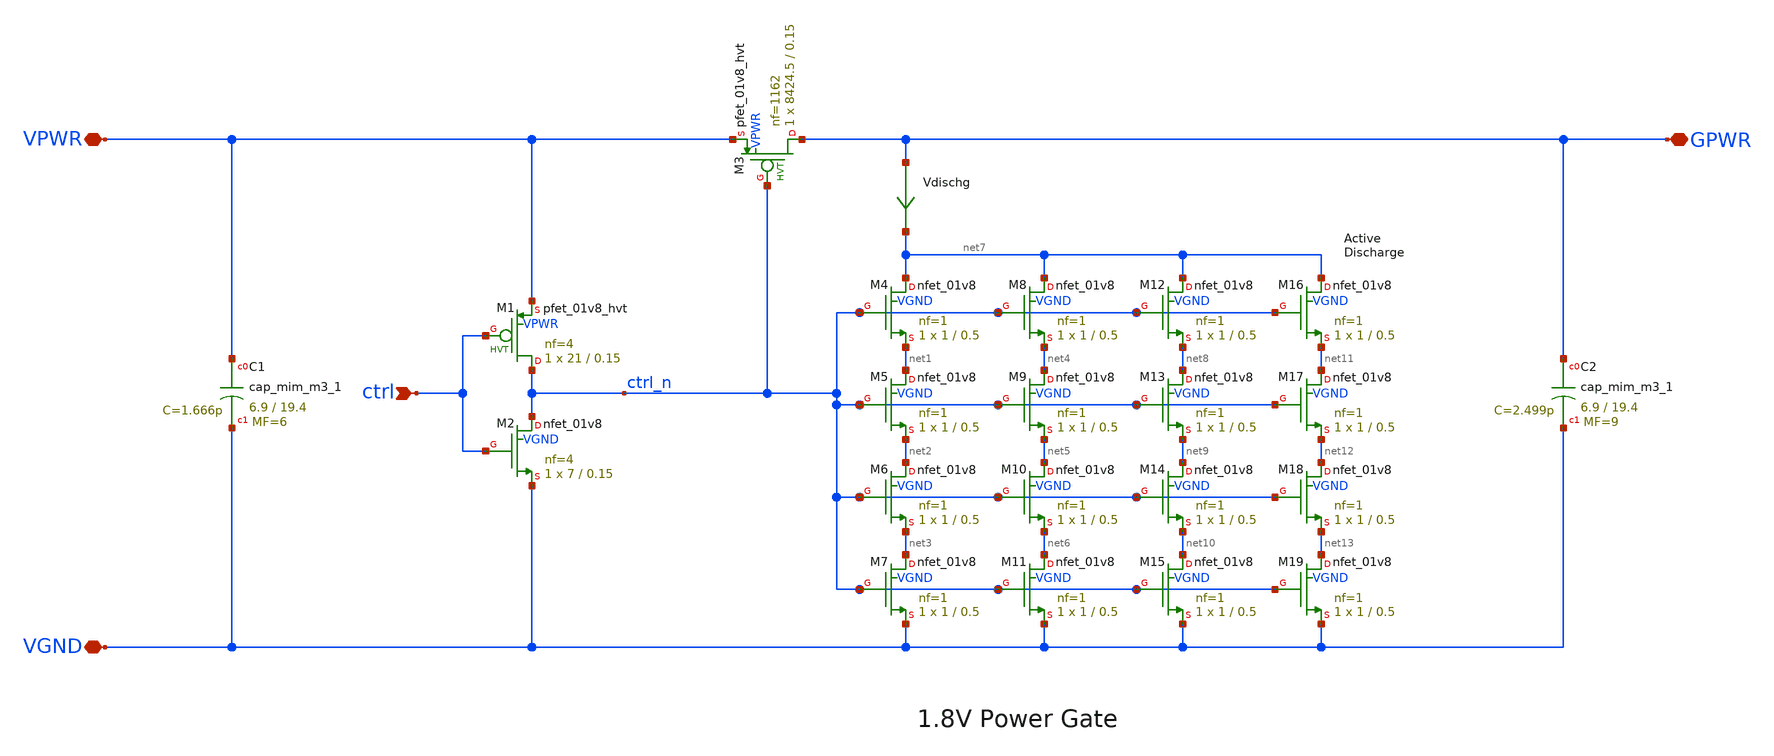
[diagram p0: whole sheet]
** sch_path: pg/sky130/tt_pg_1v8_ll_4/xschem/tt_pg_1v8_ll_4.sch
**.subckt tt_pg_1v8_ll_4 ctrl VGND VPWR GPWR
*.ipin ctrl
*.iopin VGND
*.iopin VPWR
*.iopin GPWR
XM2 ctrl_n ctrl VGND VGND sky130_fd_pr__nfet_01v8 L=0.15 W=7 nf=4 ad='int((nf+1)/2) * W/nf * 0.29' as='int((nf+2)/2) * W/nf * 0.29'
+ pd='2*int((nf+1)/2) * (W/nf + 0.29)' ps='2*int((nf+2)/2) * (W/nf + 0.29)' nrd='0.29 / W' nrs='0.29 / W'
+ sa=0 sb=0 sd=0 mult=1 m=1
XM1 ctrl_n ctrl VPWR VPWR sky130_fd_pr__pfet_01v8_hvt L=0.15 W=21 nf=4 ad='int((nf+1)/2) * W/nf * 0.29'
+ as='int((nf+2)/2) * W/nf * 0.29' pd='2*int((nf+1)/2) * (W/nf + 0.29)' ps='2*int((nf+2)/2) * (W/nf + 0.29)'
+ nrd='0.29 / W' nrs='0.29 / W' sa=0 sb=0 sd=0 mult=1 m=1
XM3 GPWR ctrl_n VPWR VPWR sky130_fd_pr__pfet_01v8_hvt L=0.15 W=8424.5 nf=1162 ad='int((nf+1)/2) * W/nf * 0.29'
+ as='int((nf+2)/2) * W/nf * 0.29' pd='2*int((nf+1)/2) * (W/nf + 0.29)' ps='2*int((nf+2)/2) * (W/nf + 0.29)'
+ nrd='0.29 / W' nrs='0.29 / W' sa=0 sb=0 sd=0 mult=1 m=1
XM4 net7 ctrl_n net1 VGND sky130_fd_pr__nfet_01v8 L=0.5 W=1 nf=1 ad='int((nf+1)/2) * W/nf * 0.29' as='int((nf+2)/2) * W/nf * 0.29'
+ pd='2*int((nf+1)/2) * (W/nf + 0.29)' ps='2*int((nf+2)/2) * (W/nf + 0.29)' nrd='0.29 / W' nrs='0.29 / W'
+ sa=0 sb=0 sd=0 mult=1 m=1
Vdischg GPWR net7 0
.save i(vdischg)
XM5 net1 ctrl_n net2 VGND sky130_fd_pr__nfet_01v8 L=0.5 W=1 nf=1 ad='int((nf+1)/2) * W/nf * 0.29' as='int((nf+2)/2) * W/nf * 0.29'
+ pd='2*int((nf+1)/2) * (W/nf + 0.29)' ps='2*int((nf+2)/2) * (W/nf + 0.29)' nrd='0.29 / W' nrs='0.29 / W'
+ sa=0 sb=0 sd=0 mult=1 m=1
XM6 net2 ctrl_n net3 VGND sky130_fd_pr__nfet_01v8 L=0.5 W=1 nf=1 ad='int((nf+1)/2) * W/nf * 0.29' as='int((nf+2)/2) * W/nf * 0.29'
+ pd='2*int((nf+1)/2) * (W/nf + 0.29)' ps='2*int((nf+2)/2) * (W/nf + 0.29)' nrd='0.29 / W' nrs='0.29 / W'
+ sa=0 sb=0 sd=0 mult=1 m=1
XM7 net3 ctrl_n VGND VGND sky130_fd_pr__nfet_01v8 L=0.5 W=1 nf=1 ad='int((nf+1)/2) * W/nf * 0.29' as='int((nf+2)/2) * W/nf * 0.29'
+ pd='2*int((nf+1)/2) * (W/nf + 0.29)' ps='2*int((nf+2)/2) * (W/nf + 0.29)' nrd='0.29 / W' nrs='0.29 / W'
+ sa=0 sb=0 sd=0 mult=1 m=1
XM8 net7 ctrl_n net4 VGND sky130_fd_pr__nfet_01v8 L=0.5 W=1 nf=1 ad='int((nf+1)/2) * W/nf * 0.29' as='int((nf+2)/2) * W/nf * 0.29'
+ pd='2*int((nf+1)/2) * (W/nf + 0.29)' ps='2*int((nf+2)/2) * (W/nf + 0.29)' nrd='0.29 / W' nrs='0.29 / W'
+ sa=0 sb=0 sd=0 mult=1 m=1
XM9 net4 ctrl_n net5 VGND sky130_fd_pr__nfet_01v8 L=0.5 W=1 nf=1 ad='int((nf+1)/2) * W/nf * 0.29' as='int((nf+2)/2) * W/nf * 0.29'
+ pd='2*int((nf+1)/2) * (W/nf + 0.29)' ps='2*int((nf+2)/2) * (W/nf + 0.29)' nrd='0.29 / W' nrs='0.29 / W'
+ sa=0 sb=0 sd=0 mult=1 m=1
XM10 net5 ctrl_n net6 VGND sky130_fd_pr__nfet_01v8 L=0.5 W=1 nf=1 ad='int((nf+1)/2) * W/nf * 0.29' as='int((nf+2)/2) * W/nf * 0.29'
+ pd='2*int((nf+1)/2) * (W/nf + 0.29)' ps='2*int((nf+2)/2) * (W/nf + 0.29)' nrd='0.29 / W' nrs='0.29 / W'
+ sa=0 sb=0 sd=0 mult=1 m=1
XM11 net6 ctrl_n VGND VGND sky130_fd_pr__nfet_01v8 L=0.5 W=1 nf=1 ad='int((nf+1)/2) * W/nf * 0.29' as='int((nf+2)/2) * W/nf * 0.29'
+ pd='2*int((nf+1)/2) * (W/nf + 0.29)' ps='2*int((nf+2)/2) * (W/nf + 0.29)' nrd='0.29 / W' nrs='0.29 / W'
+ sa=0 sb=0 sd=0 mult=1 m=1
XC1 VPWR VGND sky130_fd_pr__cap_mim_m3_1 W=6.9 L=19.4 MF=6 m=6
XC2 GPWR VGND sky130_fd_pr__cap_mim_m3_1 W=6.9 L=19.4 MF=9 m=9
XM12 net7 ctrl_n net8 VGND sky130_fd_pr__nfet_01v8 L=0.5 W=1 nf=1 ad='int((nf+1)/2) * W/nf * 0.29' as='int((nf+2)/2) * W/nf * 0.29'
+ pd='2*int((nf+1)/2) * (W/nf + 0.29)' ps='2*int((nf+2)/2) * (W/nf + 0.29)' nrd='0.29 / W' nrs='0.29 / W'
+ sa=0 sb=0 sd=0 mult=1 m=1
XM13 net8 ctrl_n net9 VGND sky130_fd_pr__nfet_01v8 L=0.5 W=1 nf=1 ad='int((nf+1)/2) * W/nf * 0.29' as='int((nf+2)/2) * W/nf * 0.29'
+ pd='2*int((nf+1)/2) * (W/nf + 0.29)' ps='2*int((nf+2)/2) * (W/nf + 0.29)' nrd='0.29 / W' nrs='0.29 / W'
+ sa=0 sb=0 sd=0 mult=1 m=1
XM14 net9 ctrl_n net10 VGND sky130_fd_pr__nfet_01v8 L=0.5 W=1 nf=1 ad='int((nf+1)/2) * W/nf * 0.29' as='int((nf+2)/2) * W/nf * 0.29'
+ pd='2*int((nf+1)/2) * (W/nf + 0.29)' ps='2*int((nf+2)/2) * (W/nf + 0.29)' nrd='0.29 / W' nrs='0.29 / W'
+ sa=0 sb=0 sd=0 mult=1 m=1
XM15 net10 ctrl_n VGND VGND sky130_fd_pr__nfet_01v8 L=0.5 W=1 nf=1 ad='int((nf+1)/2) * W/nf * 0.29' as='int((nf+2)/2) * W/nf * 0.29'
+ pd='2*int((nf+1)/2) * (W/nf + 0.29)' ps='2*int((nf+2)/2) * (W/nf + 0.29)' nrd='0.29 / W' nrs='0.29 / W'
+ sa=0 sb=0 sd=0 mult=1 m=1
XM16 net7 ctrl_n net11 VGND sky130_fd_pr__nfet_01v8 L=0.5 W=1 nf=1 ad='int((nf+1)/2) * W/nf * 0.29' as='int((nf+2)/2) * W/nf * 0.29'
+ pd='2*int((nf+1)/2) * (W/nf + 0.29)' ps='2*int((nf+2)/2) * (W/nf + 0.29)' nrd='0.29 / W' nrs='0.29 / W'
+ sa=0 sb=0 sd=0 mult=1 m=1
XM17 net11 ctrl_n net12 VGND sky130_fd_pr__nfet_01v8 L=0.5 W=1 nf=1 ad='int((nf+1)/2) * W/nf * 0.29'
+ as='int((nf+2)/2) * W/nf * 0.29' pd='2*int((nf+1)/2) * (W/nf + 0.29)' ps='2*int((nf+2)/2) * (W/nf + 0.29)'
+ nrd='0.29 / W' nrs='0.29 / W' sa=0 sb=0 sd=0 mult=1 m=1
XM18 net12 ctrl_n net13 VGND sky130_fd_pr__nfet_01v8 L=0.5 W=1 nf=1 ad='int((nf+1)/2) * W/nf * 0.29'
+ as='int((nf+2)/2) * W/nf * 0.29' pd='2*int((nf+1)/2) * (W/nf + 0.29)' ps='2*int((nf+2)/2) * (W/nf + 0.29)'
+ nrd='0.29 / W' nrs='0.29 / W' sa=0 sb=0 sd=0 mult=1 m=1
XM19 net13 ctrl_n VGND VGND sky130_fd_pr__nfet_01v8 L=0.5 W=1 nf=1 ad='int((nf+1)/2) * W/nf * 0.29' as='int((nf+2)/2) * W/nf * 0.29'
+ pd='2*int((nf+1)/2) * (W/nf + 0.29)' ps='2*int((nf+2)/2) * (W/nf + 0.29)' nrd='0.29 / W' nrs='0.29 / W'
+ sa=0 sb=0 sd=0 mult=1 m=1
**.ends
.end
